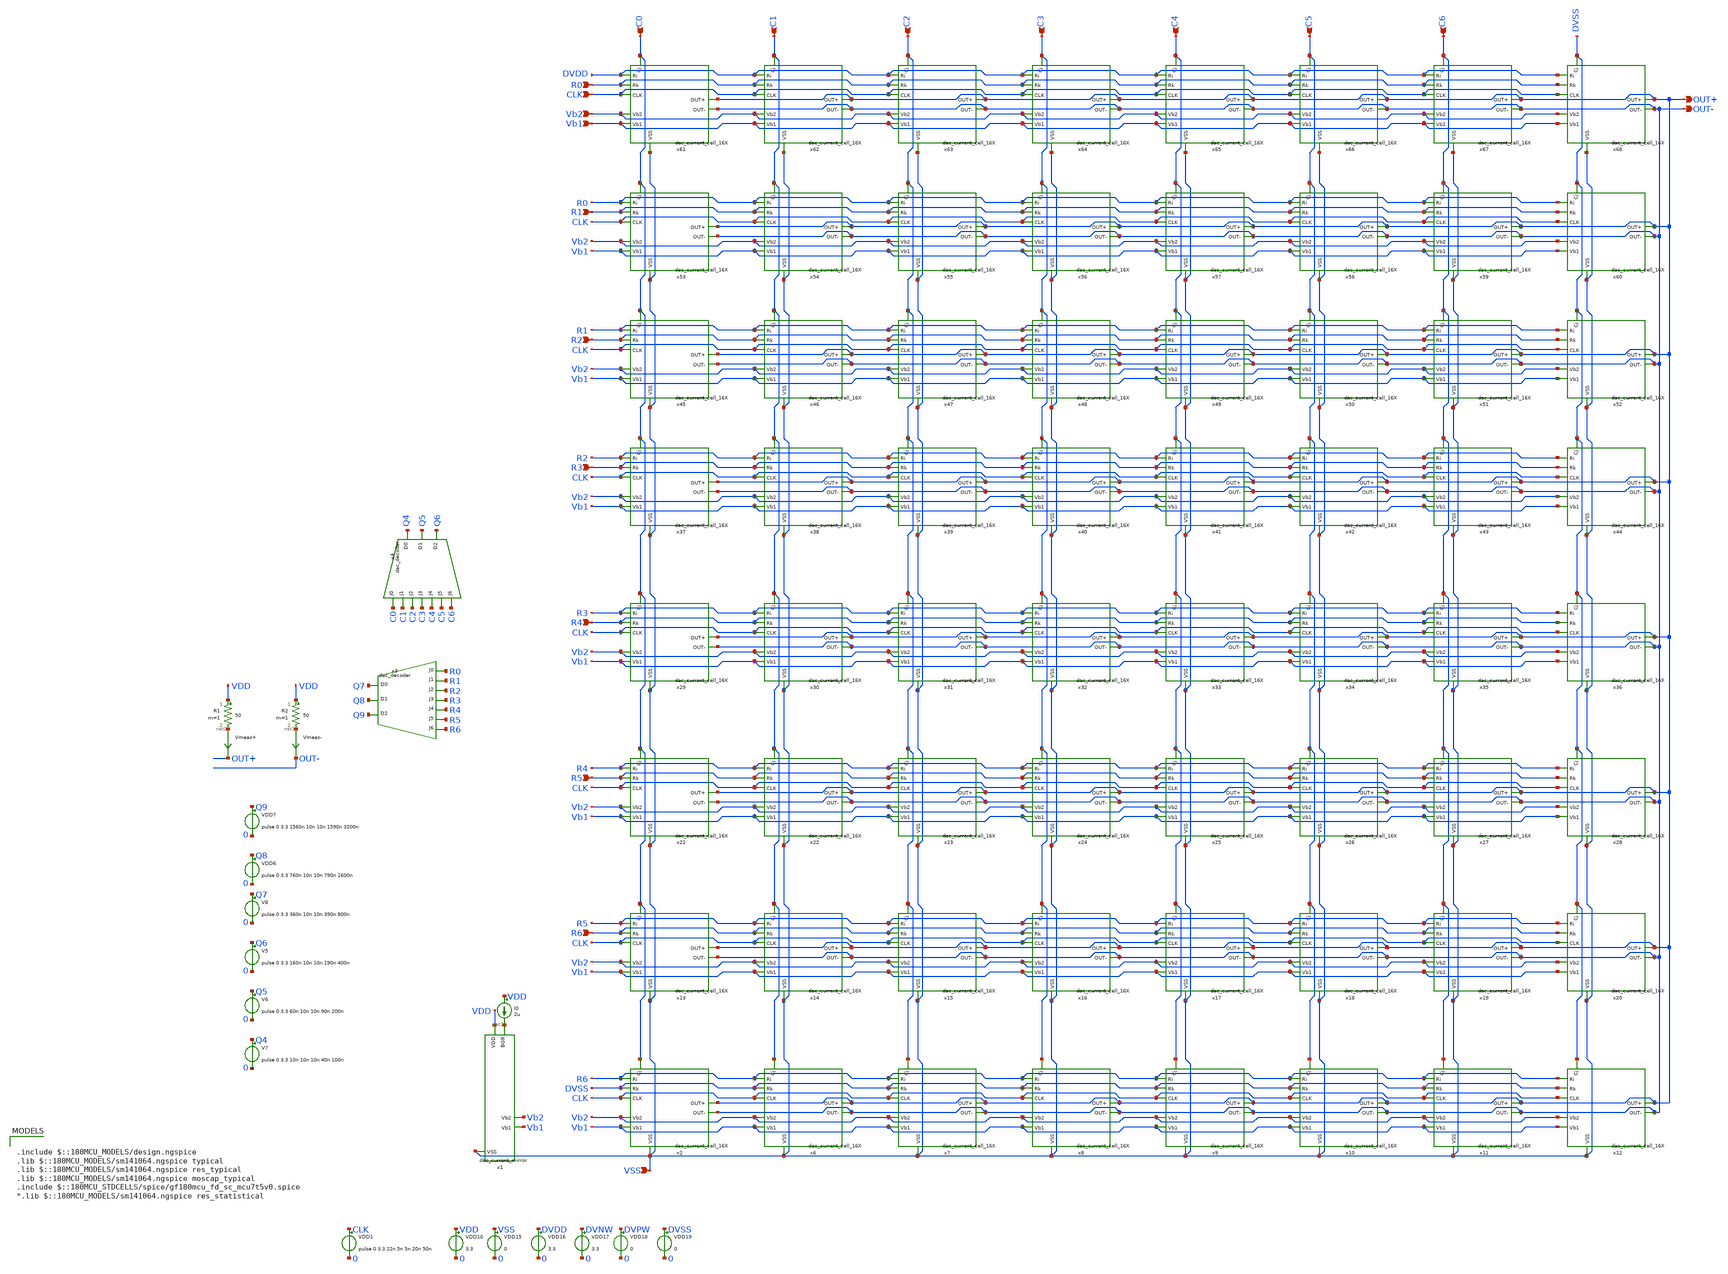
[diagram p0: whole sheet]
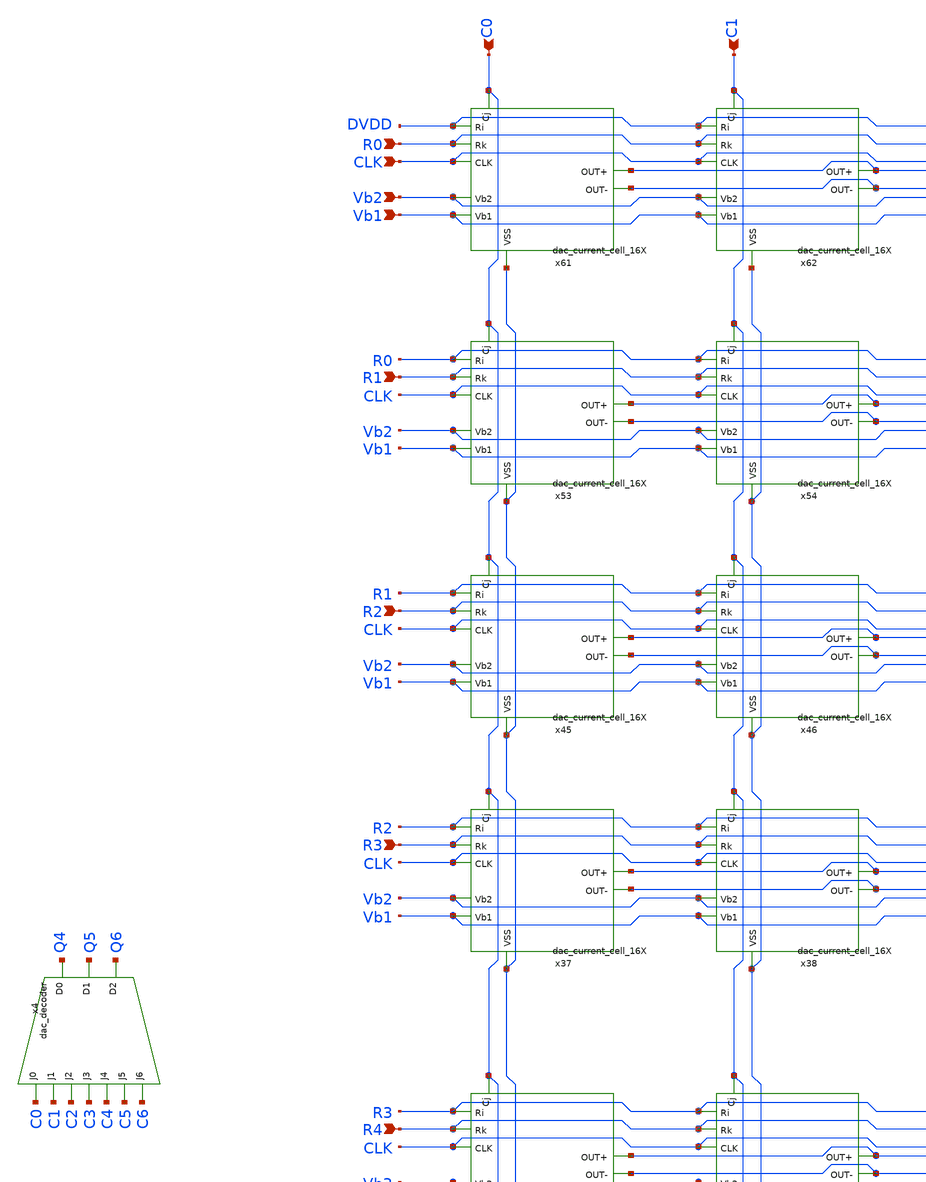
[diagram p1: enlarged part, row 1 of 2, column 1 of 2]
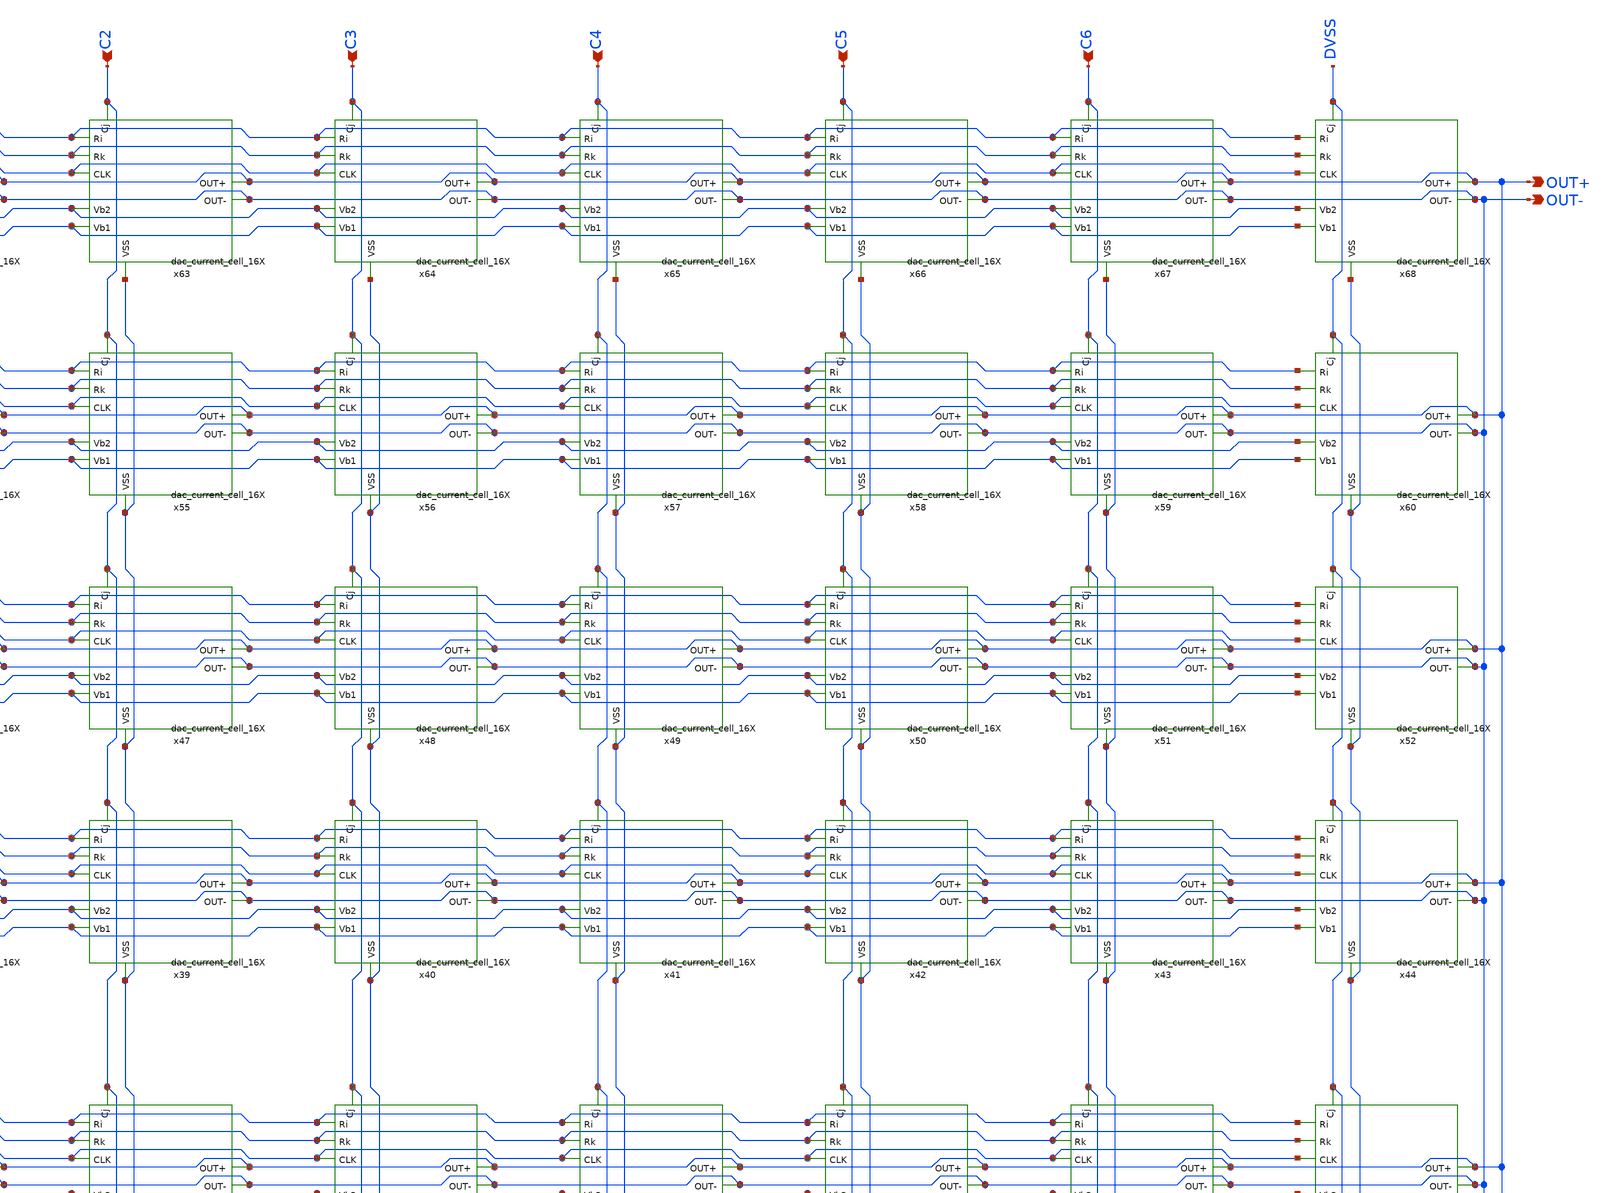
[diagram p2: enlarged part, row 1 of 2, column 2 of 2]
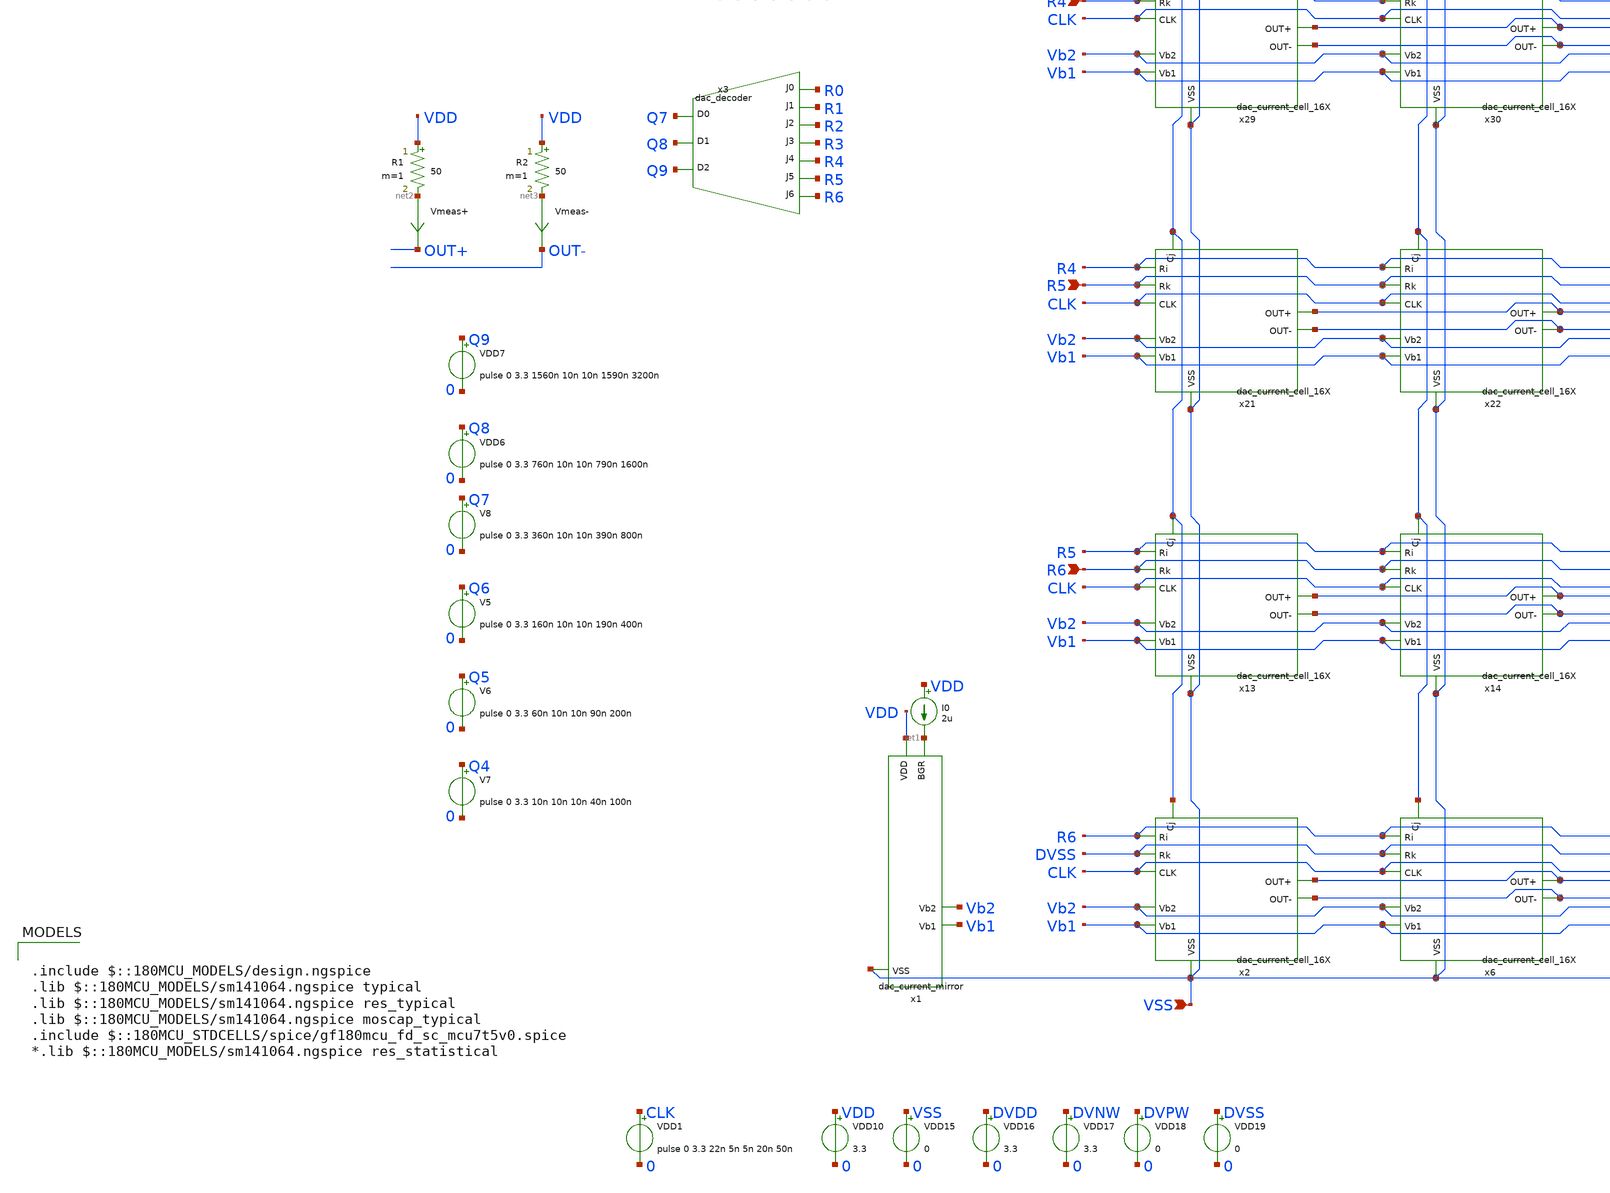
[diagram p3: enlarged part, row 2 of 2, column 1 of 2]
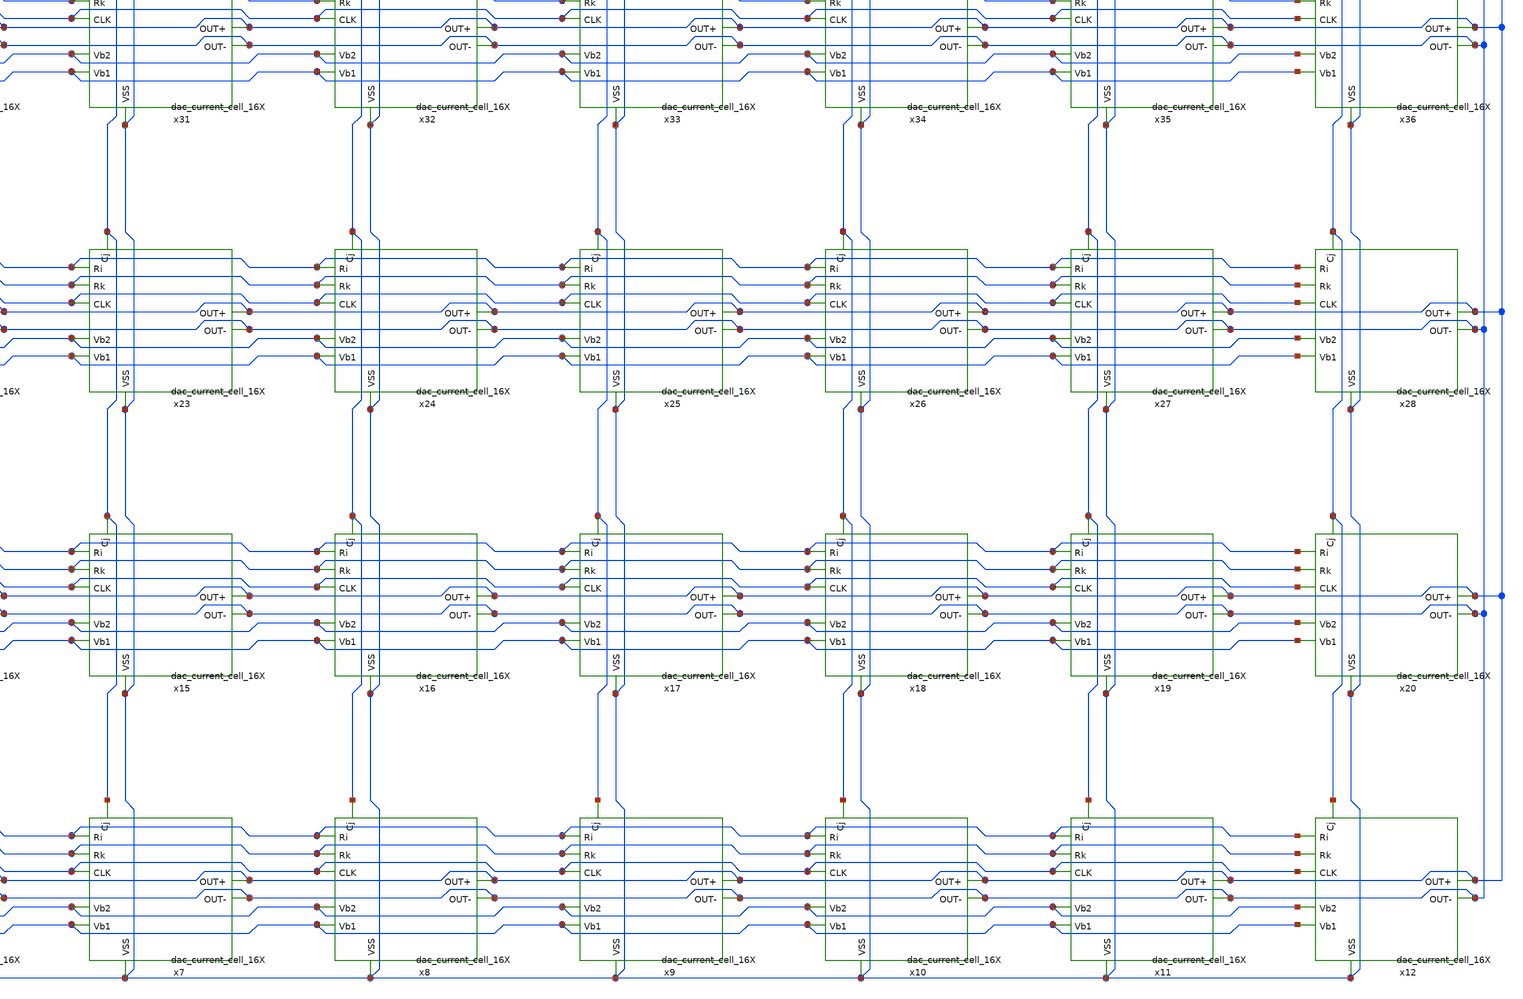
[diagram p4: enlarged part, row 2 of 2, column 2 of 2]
** sch_path: DAC/xschem/test_rawdac_msb_matrix.sch
**.subckt test_rawdac_msb_matrix R0 CLK R1 R2 R3 R4 R5 R6 C0 C1 C2 C3 C4 C5 C6 Vb2 Vb1 OUT+ OUT- VSS
*.ipin R0
*.ipin CLK
*.ipin R1
*.ipin R2
*.ipin R3
*.ipin R4
*.ipin R5
*.ipin R6
*.ipin C0
*.ipin C1
*.ipin C2
*.ipin C3
*.ipin C4
*.ipin C5
*.ipin C6
*.ipin Vb2
*.ipin Vb1
*.opin OUT+
*.opin OUT-
*.ipin VSS
VDD6 Q8 0 pulse 0 3.3 760n 10n 10n 790n 1600n
VDD7 Q9 0 pulse 0 3.3 1560n 10n 10n 1590n 3200n
VDD10 VDD 0 3.3
VDD15 VSS 0 0
VDD16 DVDD 0 3.3
VDD17 DVNW 0 3.3
VDD18 DVPW 0 0
VDD19 DVSS 0 0
I0 VDD net1 2u
R1 VDD net2 50 m=1
R2 VDD net3 50 m=1
Vmeas+ net2 OUT+ 0
.save i(vmeas+)
Vmeas- net3 OUT- 0
.save i(vmeas-)
x2 C0 R6 OUT+ OUT- CLK DVSS Vb2 Vb1 VSS DVDD DVNW DVPW DVSS dac_current_cell_16X
x6 C1 R6 OUT+ OUT- CLK DVSS Vb2 Vb1 VSS DVDD DVNW DVPW DVSS dac_current_cell_16X
x7 C2 R6 OUT+ OUT- CLK DVSS Vb2 Vb1 VSS DVDD DVNW DVPW DVSS dac_current_cell_16X
x8 C3 R6 OUT+ OUT- CLK DVSS Vb2 Vb1 VSS DVDD DVNW DVPW DVSS dac_current_cell_16X
x9 C4 R6 OUT+ OUT- CLK DVSS Vb2 Vb1 VSS DVDD DVNW DVPW DVSS dac_current_cell_16X
x10 C5 R6 OUT+ OUT- CLK DVSS Vb2 Vb1 VSS DVDD DVNW DVPW DVSS dac_current_cell_16X
x11 C6 R6 OUT+ OUT- CLK DVSS Vb2 Vb1 VSS DVDD DVNW DVPW DVSS dac_current_cell_16X
x12 DVSS R6 OUT+ OUT- CLK DVSS Vb2 Vb1 VSS DVDD DVNW DVPW DVSS dac_current_cell_16X
x13 C0 R5 OUT+ OUT- CLK R6 Vb2 Vb1 VSS DVDD DVNW DVPW DVSS dac_current_cell_16X
x14 C1 R5 OUT+ OUT- CLK R6 Vb2 Vb1 VSS DVDD DVNW DVPW DVSS dac_current_cell_16X
x15 C2 R5 OUT+ OUT- CLK R6 Vb2 Vb1 VSS DVDD DVNW DVPW DVSS dac_current_cell_16X
x16 C3 R5 OUT+ OUT- CLK R6 Vb2 Vb1 VSS DVDD DVNW DVPW DVSS dac_current_cell_16X
x17 C4 R5 OUT+ OUT- CLK R6 Vb2 Vb1 VSS DVDD DVNW DVPW DVSS dac_current_cell_16X
x18 C5 R5 OUT+ OUT- CLK R6 Vb2 Vb1 VSS DVDD DVNW DVPW DVSS dac_current_cell_16X
x19 C6 R5 OUT+ OUT- CLK R6 Vb2 Vb1 VSS DVDD DVNW DVPW DVSS dac_current_cell_16X
x20 DVSS R5 OUT+ OUT- CLK R6 Vb2 Vb1 VSS DVDD DVNW DVPW DVSS dac_current_cell_16X
x21 C0 R4 OUT+ OUT- CLK R5 Vb2 Vb1 VSS DVDD DVNW DVPW DVSS dac_current_cell_16X
x22 C1 R4 OUT+ OUT- CLK R5 Vb2 Vb1 VSS DVDD DVNW DVPW DVSS dac_current_cell_16X
x23 C2 R4 OUT+ OUT- CLK R5 Vb2 Vb1 VSS DVDD DVNW DVPW DVSS dac_current_cell_16X
x24 C3 R4 OUT+ OUT- CLK R5 Vb2 Vb1 VSS DVDD DVNW DVPW DVSS dac_current_cell_16X
x25 C4 R4 OUT+ OUT- CLK R5 Vb2 Vb1 VSS DVDD DVNW DVPW DVSS dac_current_cell_16X
x26 C5 R4 OUT+ OUT- CLK R5 Vb2 Vb1 VSS DVDD DVNW DVPW DVSS dac_current_cell_16X
x27 C6 R4 OUT+ OUT- CLK R5 Vb2 Vb1 VSS DVDD DVNW DVPW DVSS dac_current_cell_16X
x28 DVSS R4 OUT+ OUT- CLK R5 Vb2 Vb1 VSS DVDD DVNW DVPW DVSS dac_current_cell_16X
x29 C0 R3 OUT+ OUT- CLK R4 Vb2 Vb1 VSS DVDD DVNW DVPW DVSS dac_current_cell_16X
x30 C1 R3 OUT+ OUT- CLK R4 Vb2 Vb1 VSS DVDD DVNW DVPW DVSS dac_current_cell_16X
x31 C2 R3 OUT+ OUT- CLK R4 Vb2 Vb1 VSS DVDD DVNW DVPW DVSS dac_current_cell_16X
x32 C3 R3 OUT+ OUT- CLK R4 Vb2 Vb1 VSS DVDD DVNW DVPW DVSS dac_current_cell_16X
x33 C4 R3 OUT+ OUT- CLK R4 Vb2 Vb1 VSS DVDD DVNW DVPW DVSS dac_current_cell_16X
x34 C5 R3 OUT+ OUT- CLK R4 Vb2 Vb1 VSS DVDD DVNW DVPW DVSS dac_current_cell_16X
x35 C6 R3 OUT+ OUT- CLK R4 Vb2 Vb1 VSS DVDD DVNW DVPW DVSS dac_current_cell_16X
x36 DVSS R3 OUT+ OUT- CLK R4 Vb2 Vb1 VSS DVDD DVNW DVPW DVSS dac_current_cell_16X
x37 C0 R2 OUT+ OUT- CLK R3 Vb2 Vb1 VSS DVDD DVNW DVPW DVSS dac_current_cell_16X
x38 C1 R2 OUT+ OUT- CLK R3 Vb2 Vb1 VSS DVDD DVNW DVPW DVSS dac_current_cell_16X
x39 C2 R2 OUT+ OUT- CLK R3 Vb2 Vb1 VSS DVDD DVNW DVPW DVSS dac_current_cell_16X
x40 C3 R2 OUT+ OUT- CLK R3 Vb2 Vb1 VSS DVDD DVNW DVPW DVSS dac_current_cell_16X
x41 C4 R2 OUT+ OUT- CLK R3 Vb2 Vb1 VSS DVDD DVNW DVPW DVSS dac_current_cell_16X
x42 C5 R2 OUT+ OUT- CLK R3 Vb2 Vb1 VSS DVDD DVNW DVPW DVSS dac_current_cell_16X
x43 C6 R2 OUT+ OUT- CLK R3 Vb2 Vb1 VSS DVDD DVNW DVPW DVSS dac_current_cell_16X
x44 DVSS R2 OUT+ OUT- CLK R3 Vb2 Vb1 VSS DVDD DVNW DVPW DVSS dac_current_cell_16X
x45 C0 R1 OUT+ OUT- CLK R2 Vb2 Vb1 VSS DVDD DVNW DVPW DVSS dac_current_cell_16X
x46 C1 R1 OUT+ OUT- CLK R2 Vb2 Vb1 VSS DVDD DVNW DVPW DVSS dac_current_cell_16X
x47 C2 R1 OUT+ OUT- CLK R2 Vb2 Vb1 VSS DVDD DVNW DVPW DVSS dac_current_cell_16X
x48 C3 R1 OUT+ OUT- CLK R2 Vb2 Vb1 VSS DVDD DVNW DVPW DVSS dac_current_cell_16X
x49 C4 R1 OUT+ OUT- CLK R2 Vb2 Vb1 VSS DVDD DVNW DVPW DVSS dac_current_cell_16X
x50 C5 R1 OUT+ OUT- CLK R2 Vb2 Vb1 VSS DVDD DVNW DVPW DVSS dac_current_cell_16X
x51 C6 R1 OUT+ OUT- CLK R2 Vb2 Vb1 VSS DVDD DVNW DVPW DVSS dac_current_cell_16X
x52 DVSS R1 OUT+ OUT- CLK R2 Vb2 Vb1 VSS DVDD DVNW DVPW DVSS dac_current_cell_16X
x53 C0 R0 OUT+ OUT- CLK R1 Vb2 Vb1 VSS DVDD DVNW DVPW DVSS dac_current_cell_16X
x54 C1 R0 OUT+ OUT- CLK R1 Vb2 Vb1 VSS DVDD DVNW DVPW DVSS dac_current_cell_16X
x55 C2 R0 OUT+ OUT- CLK R1 Vb2 Vb1 VSS DVDD DVNW DVPW DVSS dac_current_cell_16X
x56 C3 R0 OUT+ OUT- CLK R1 Vb2 Vb1 VSS DVDD DVNW DVPW DVSS dac_current_cell_16X
x57 C4 R0 OUT+ OUT- CLK R1 Vb2 Vb1 VSS DVDD DVNW DVPW DVSS dac_current_cell_16X
x58 C5 R0 OUT+ OUT- CLK R1 Vb2 Vb1 VSS DVDD DVNW DVPW DVSS dac_current_cell_16X
x59 C6 R0 OUT+ OUT- CLK R1 Vb2 Vb1 VSS DVDD DVNW DVPW DVSS dac_current_cell_16X
x60 DVSS R0 OUT+ OUT- CLK R1 Vb2 Vb1 VSS DVDD DVNW DVPW DVSS dac_current_cell_16X
x61 C0 DVDD OUT+ OUT- CLK R0 Vb2 Vb1 VSS DVDD DVNW DVPW DVSS dac_current_cell_16X
x62 C1 DVDD OUT+ OUT- CLK R0 Vb2 Vb1 VSS DVDD DVNW DVPW DVSS dac_current_cell_16X
x63 C2 DVDD OUT+ OUT- CLK R0 Vb2 Vb1 VSS DVDD DVNW DVPW DVSS dac_current_cell_16X
x64 C3 DVDD OUT+ OUT- CLK R0 Vb2 Vb1 VSS DVDD DVNW DVPW DVSS dac_current_cell_16X
x65 C4 DVDD OUT+ OUT- CLK R0 Vb2 Vb1 VSS DVDD DVNW DVPW DVSS dac_current_cell_16X
x66 C5 DVDD OUT+ OUT- CLK R0 Vb2 Vb1 VSS DVDD DVNW DVPW DVSS dac_current_cell_16X
x67 C6 DVDD OUT+ OUT- CLK R0 Vb2 Vb1 VSS DVDD DVNW DVPW DVSS dac_current_cell_16X
x68 DVSS DVDD OUT+ OUT- CLK R0 Vb2 Vb1 VSS DVDD DVNW DVPW DVSS dac_current_cell_16X
x1 VDD net1 Vb2 Vb1 VSS dac_current_mirror
x3 R6 R5 R4 R3 R2 R1 Q9 Q8 Q7 R0 VDD VNW VPW VSS dac_decoder
x4 C6 C5 C4 C3 C2 C1 Q6 Q5 Q4 C0 VDD VNW VPW VSS dac_decoder
V5 Q6 0 pulse 0 3.3 160n 10n 10n 190n 400n
V6 Q5 0 pulse 0 3.3 60n 10n 10n 90n 200n
V7 Q4 0 pulse 0 3.3 10n 10n 10n 40n 100n
V8 Q7 0 pulse 0 3.3 360n 10n 10n 390n 800n
VDD1 CLK 0 pulse 0 3.3 22n 5n 5n 20n 50n
**** begin user architecture code




.control
	tran 1n 3200n
	plot i(Vmeas+) i(Vmeas-)
	write test_dac_MSB.raw
.endc
.save all





.include $::180MCU_MODELS/design.ngspice
.lib $::180MCU_MODELS/sm141064.ngspice typical
.lib $::180MCU_MODELS/sm141064.ngspice res_typical
.lib $::180MCU_MODELS/sm141064.ngspice moscap_typical
.include $::180MCU_STDCELLS/spice/gf180mcu_fd_sc_mcu7t5v0.spice
*.lib $::180MCU_MODELS/sm141064.ngspice res_statistical

**** end user architecture code
**.ends
.end
